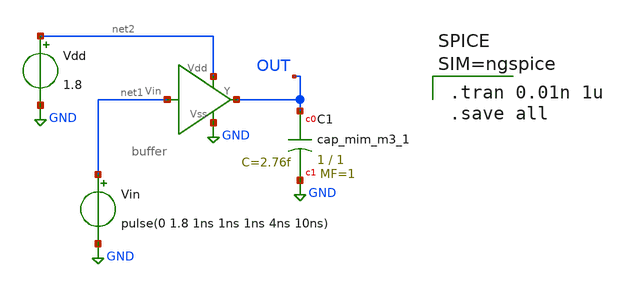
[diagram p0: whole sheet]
** sch_path: buffer/buffer_hierarchical.sch
**.subckt buffer_hierarchical
Vdd net2 GND 1.8
Vin net1 GND pulse(0 1.8 1ns 1ns 1ns 4ns 10ns)
XC1 OUT GND sky130_fd_pr__cap_mim_m3_1 W=1 L=1 MF=1 m=1
x1 GND net1 net2 OUT buffer
**** begin user architecture code


.tran 0.01n 1u
.save all



** opencircuitdesign pdks install
.lib $::SKYWATER_MODELS/sky130.lib.spice tt


**** end user architecture code
**.ends
.GLOBAL GND
.end
